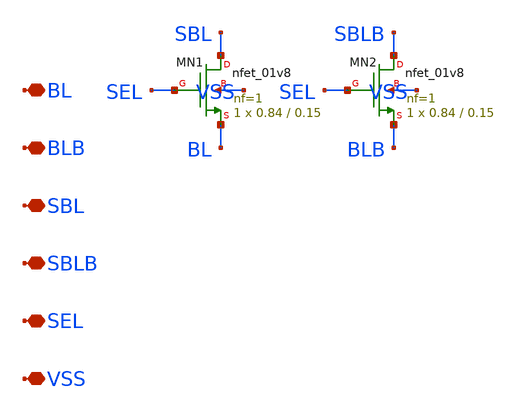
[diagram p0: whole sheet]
** sch_path: design/compiler/cells/sram_colmux.sch
**.subckt sram_colmux BL BLB SBL SBLB SEL VSS
*.iopin BL
*.iopin BLB
*.iopin SBL
*.iopin SBLB
*.iopin SEL
*.iopin VSS
XMN1 SBL SEL BL VSS sky130_fd_pr__nfet_01v8 L=0.15 W=0.84 nf=1 ad=0.2436 as=0.2436 pd=2.26 ps=2.26
+ nrd=0.3452 nrs=0.3452 sa=0 sb=0 sd=0 mult=1 m=1
XMN2 SBLB SEL BLB VSS sky130_fd_pr__nfet_01v8 L=0.15 W=0.84 nf=1 ad=0.2436 as=0.2436 pd=2.26 ps=2.26
+ nrd=0.3452 nrs=0.3452 sa=0 sb=0 sd=0 mult=1 m=1
**.ends
.end
